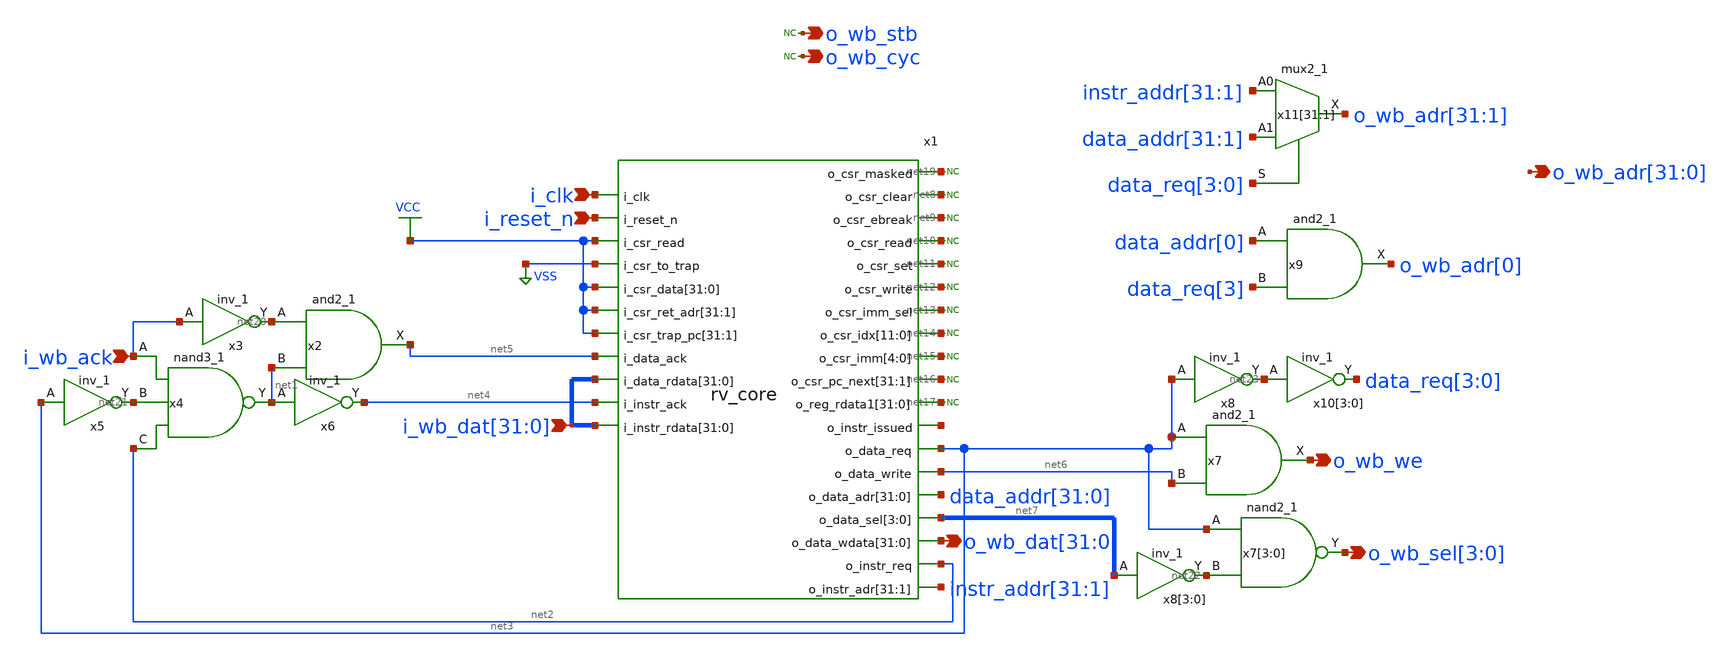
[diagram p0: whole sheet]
** sch_path: blocks/rv_core_wb/rv_core_wb.sch
**.subckt rv_core_wb i_clk i_reset_n i_wb_ack o_wb_we
*+ o_wb_sel[3],o_wb_sel[2],o_wb_sel[1],o_wb_sel[0] o_wb_stb o_wb_cyc
*+ o_wb_adr[31],o_wb_adr[30],o_wb_adr[29],o_wb_adr[28],o_wb_adr[27],o_wb_adr[26],o_wb_adr[25],o_wb_adr[24],o_wb_adr[23],o_wb_adr[22],o_wb_adr[21],o_wb_adr[20],o_wb_adr[19],o_wb_adr[18],o_wb_adr[17],o_wb_adr[16],o_wb_adr[15],o_wb_adr[14],o_wb_adr[13],o_wb_adr[12],o_wb_adr[11],o_wb_adr[10],o_wb_adr[9],o_wb_adr[8],o_wb_adr[7],o_wb_adr[6],o_wb_adr[5],o_wb_adr[4],o_wb_adr[3],o_wb_adr[2],o_wb_adr[1],o_wb_adr[0]
*+ o_wb_dat[31],o_wb_dat[30],o_wb_dat[29],o_wb_dat[28],o_wb_dat[27],o_wb_dat[26],o_wb_dat[25],o_wb_dat[24],o_wb_dat[23],o_wb_dat[22],o_wb_dat[21],o_wb_dat[20],o_wb_dat[19],o_wb_dat[18],o_wb_dat[17],o_wb_dat[16],o_wb_dat[15],o_wb_dat[14],o_wb_dat[13],o_wb_dat[12],o_wb_dat[11],o_wb_dat[10],o_wb_dat[9],o_wb_dat[8],o_wb_dat[7],o_wb_dat[6],o_wb_dat[5],o_wb_dat[4],o_wb_dat[3],o_wb_dat[2],o_wb_dat[1],o_wb_dat[0]
*+ i_wb_dat[31],i_wb_dat[30],i_wb_dat[29],i_wb_dat[28],i_wb_dat[27],i_wb_dat[26],i_wb_dat[25],i_wb_dat[24],i_wb_dat[23],i_wb_dat[22],i_wb_dat[21],i_wb_dat[20],i_wb_dat[19],i_wb_dat[18],i_wb_dat[17],i_wb_dat[16],i_wb_dat[15],i_wb_dat[14],i_wb_dat[13],i_wb_dat[12],i_wb_dat[11],i_wb_dat[10],i_wb_dat[9],i_wb_dat[8],i_wb_dat[7],i_wb_dat[6],i_wb_dat[5],i_wb_dat[4],i_wb_dat[3],i_wb_dat[2],i_wb_dat[1],i_wb_dat[0]
*.ipin i_clk
*.ipin i_reset_n
*.ipin i_wb_ack
*.opin o_wb_we
*.opin o_wb_sel[3],o_wb_sel[2],o_wb_sel[1],o_wb_sel[0]
*.opin o_wb_stb
*.opin o_wb_cyc
*.opin
*+ o_wb_adr[31],o_wb_adr[30],o_wb_adr[29],o_wb_adr[28],o_wb_adr[27],o_wb_adr[26],o_wb_adr[25],o_wb_adr[24],o_wb_adr[23],o_wb_adr[22],o_wb_adr[21],o_wb_adr[20],o_wb_adr[19],o_wb_adr[18],o_wb_adr[17],o_wb_adr[16],o_wb_adr[15],o_wb_adr[14],o_wb_adr[13],o_wb_adr[12],o_wb_adr[11],o_wb_adr[10],o_wb_adr[9],o_wb_adr[8],o_wb_adr[7],o_wb_adr[6],o_wb_adr[5],o_wb_adr[4],o_wb_adr[3],o_wb_adr[2],o_wb_adr[1],o_wb_adr[0]
*.opin
*+ o_wb_dat[31],o_wb_dat[30],o_wb_dat[29],o_wb_dat[28],o_wb_dat[27],o_wb_dat[26],o_wb_dat[25],o_wb_dat[24],o_wb_dat[23],o_wb_dat[22],o_wb_dat[21],o_wb_dat[20],o_wb_dat[19],o_wb_dat[18],o_wb_dat[17],o_wb_dat[16],o_wb_dat[15],o_wb_dat[14],o_wb_dat[13],o_wb_dat[12],o_wb_dat[11],o_wb_dat[10],o_wb_dat[9],o_wb_dat[8],o_wb_dat[7],o_wb_dat[6],o_wb_dat[5],o_wb_dat[4],o_wb_dat[3],o_wb_dat[2],o_wb_dat[1],o_wb_dat[0]
*.ipin
*+ i_wb_dat[31],i_wb_dat[30],i_wb_dat[29],i_wb_dat[28],i_wb_dat[27],i_wb_dat[26],i_wb_dat[25],i_wb_dat[24],i_wb_dat[23],i_wb_dat[22],i_wb_dat[21],i_wb_dat[20],i_wb_dat[19],i_wb_dat[18],i_wb_dat[17],i_wb_dat[16],i_wb_dat[15],i_wb_dat[14],i_wb_dat[13],i_wb_dat[12],i_wb_dat[11],i_wb_dat[10],i_wb_dat[9],i_wb_dat[8],i_wb_dat[7],i_wb_dat[6],i_wb_dat[5],i_wb_dat[4],i_wb_dat[3],i_wb_dat[2],i_wb_dat[1],i_wb_dat[0]
x1 net8 i_clk net9 i_reset_n VCC net10 net11 VSS net12 VCC VCC VCC VCC VCC VCC VCC VCC VCC VCC VCC
+ VCC VCC VCC VCC VCC VCC VCC VCC VCC VCC VCC VCC VCC VCC VCC VCC VCC VCC VCC VCC VCC VCC VCC VCC VCC VCC
+ VCC VCC VCC VCC VCC VCC VCC VCC VCC VCC VCC VCC VCC VCC VCC VCC VCC VCC VCC VCC VCC VCC VCC VCC VCC VCC
+ net13 net14 net14 net14 net14 net14 net14 net14 net14 net14 net14 net14 net14 VCC VCC VCC VCC VCC VCC VCC
+ VCC VCC VCC VCC VCC VCC VCC VCC VCC VCC VCC VCC VCC VCC VCC VCC VCC VCC VCC VCC VCC VCC VCC VCC net15
+ net15 net15 net15 net15 net16 net16 net16 net16 net16 net16 net16 net16 net16 net16 net16 net16 net16
+ net16 net16 net16 net16 net16 net16 net16 net16 net16 net16 net16 net16 net16 net16 net16 net16 net16
+ net16 net17 net17 net17 net17 net17 net17 net17 net17 net17 net17 net17 net17 net17 net17 net17 net17
+ net17 net17 net17 net17 net17 net17 net17 net17 net17 net17 net17 net17 net17 net17 net17 net17 net18
+ net3 net5 net6 i_wb_dat[31] i_wb_dat[30] i_wb_dat[29] i_wb_dat[28] i_wb_dat[27] i_wb_dat[26]
+ i_wb_dat[25] i_wb_dat[24] i_wb_dat[23] i_wb_dat[22] i_wb_dat[21] i_wb_dat[20] i_wb_dat[19] i_wb_dat[18]
+ i_wb_dat[17] i_wb_dat[16] i_wb_dat[15] i_wb_dat[14] i_wb_dat[13] i_wb_dat[12] i_wb_dat[11] i_wb_dat[10]
+ i_wb_dat[9] i_wb_dat[8] i_wb_dat[7] i_wb_dat[6] i_wb_dat[5] i_wb_dat[4] i_wb_dat[3] i_wb_dat[2] i_wb_dat[1]
+ i_wb_dat[0] data_addr[31] data_addr[30] data_addr[29] data_addr[28] data_addr[27] data_addr[26] data_addr[25]
+ data_addr[24] data_addr[23] data_addr[22] data_addr[21] data_addr[20] data_addr[19] data_addr[18] data_addr[17]
+ data_addr[16] data_addr[15] data_addr[14] data_addr[13] data_addr[12] data_addr[11] data_addr[10] data_addr[9]
+ data_addr[8] data_addr[7] data_addr[6] data_addr[5] data_addr[4] data_addr[3] data_addr[2] data_addr[1]
+ data_addr[0] net7[3] net7[2] net7[1] net7[0] o_wb_dat[31] o_wb_dat[30] o_wb_dat[29] o_wb_dat[28] o_wb_dat[27]
+ o_wb_dat[26] o_wb_dat[25] o_wb_dat[24] o_wb_dat[23] o_wb_dat[22] o_wb_dat[21] o_wb_dat[20] o_wb_dat[19]
+ o_wb_dat[18] o_wb_dat[17] o_wb_dat[16] o_wb_dat[15] o_wb_dat[14] o_wb_dat[13] o_wb_dat[12] o_wb_dat[11]
+ o_wb_dat[10] o_wb_dat[9] o_wb_dat[8] o_wb_dat[7] o_wb_dat[6] o_wb_dat[5] o_wb_dat[4] o_wb_dat[3] o_wb_dat[2]
+ o_wb_dat[1] o_wb_dat[0] net2 net4 instr_addr[31] instr_addr[30] instr_addr[29] instr_addr[28] instr_addr[27]
+ instr_addr[26] instr_addr[25] instr_addr[24] instr_addr[23] instr_addr[22] instr_addr[21] instr_addr[20]
+ instr_addr[19] instr_addr[18] instr_addr[17] instr_addr[16] instr_addr[15] instr_addr[14] instr_addr[13]
+ instr_addr[12] instr_addr[11] instr_addr[10] instr_addr[9] instr_addr[8] instr_addr[7] instr_addr[6] instr_addr[5]
+ instr_addr[4] instr_addr[3] instr_addr[2] instr_addr[1] i_wb_dat[31] i_wb_dat[30] i_wb_dat[29] i_wb_dat[28]
+ i_wb_dat[27] i_wb_dat[26] i_wb_dat[25] i_wb_dat[24] i_wb_dat[23] i_wb_dat[22] i_wb_dat[21] i_wb_dat[20]
+ i_wb_dat[19] i_wb_dat[18] i_wb_dat[17] i_wb_dat[16] i_wb_dat[15] i_wb_dat[14] i_wb_dat[13] i_wb_dat[12]
+ i_wb_dat[11] i_wb_dat[10] i_wb_dat[9] i_wb_dat[8] i_wb_dat[7] i_wb_dat[6] i_wb_dat[5] i_wb_dat[4] i_wb_dat[3]
+ i_wb_dat[2] i_wb_dat[1] i_wb_dat[0] net19 rv_core
x2 net20 net1 VSS VSS VCC VCC net5 sky130_fd_sc_hs__and2_1
x3 i_wb_ack VSS VSS VCC VCC net20 sky130_fd_sc_hs__inv_1
x4 i_wb_ack net21 net2 VSS VSS VCC VCC net1 sky130_fd_sc_hs__nand3_1
x5 net3 VSS VSS VCC VCC net21 sky130_fd_sc_hs__inv_1
x6 net1 VSS VSS VCC VCC net4 sky130_fd_sc_hs__inv_1
* noconn #net8
* noconn #net9
* noconn #net10
* noconn #net11
* noconn #net12
* noconn #net13
* noconn #net14
* noconn #net15
* noconn #net16
* noconn #net17
x7 net3 net6 VSS VSS VCC VCC o_wb_we sky130_fd_sc_hs__and2_1
x8[3] net7[3] VSS VSS VCC VCC net22[3] sky130_fd_sc_hs__inv_1
x8[2] net7[2] VSS VSS VCC VCC net22[2] sky130_fd_sc_hs__inv_1
x8[1] net7[1] VSS VSS VCC VCC net22[1] sky130_fd_sc_hs__inv_1
x8[0] net7[0] VSS VSS VCC VCC net22[0] sky130_fd_sc_hs__inv_1
x7[3] net3 net22[3] VSS VSS VCC VCC o_wb_sel[3] sky130_fd_sc_hs__nand2_1
x7[2] net3 net22[2] VSS VSS VCC VCC o_wb_sel[2] sky130_fd_sc_hs__nand2_1
x7[1] net3 net22[1] VSS VSS VCC VCC o_wb_sel[1] sky130_fd_sc_hs__nand2_1
x7[0] net3 net22[0] VSS VSS VCC VCC o_wb_sel[0] sky130_fd_sc_hs__nand2_1
x8 net3 VSS VSS VCC VCC net23 sky130_fd_sc_hs__inv_1
x10[3] net23 VSS VSS VCC VCC data_req[3] sky130_fd_sc_hs__inv_1
x10[2] net23 VSS VSS VCC VCC data_req[2] sky130_fd_sc_hs__inv_1
x10[1] net23 VSS VSS VCC VCC data_req[1] sky130_fd_sc_hs__inv_1
x10[0] net23 VSS VSS VCC VCC data_req[0] sky130_fd_sc_hs__inv_1
x9 data_addr[0] data_req[3] VSS VSS VCC VCC o_wb_adr[0] sky130_fd_sc_hs__and2_1
x11[31] instr_addr[31] data_addr[31] data_req[3] VSS VSS VCC VCC o_wb_adr[31]
+ sky130_fd_sc_hs__mux2_1
x11[30] instr_addr[30] data_addr[30] data_req[2] VSS VSS VCC VCC o_wb_adr[30]
+ sky130_fd_sc_hs__mux2_1
x11[29] instr_addr[29] data_addr[29] data_req[1] VSS VSS VCC VCC o_wb_adr[29]
+ sky130_fd_sc_hs__mux2_1
x11[28] instr_addr[28] data_addr[28] data_req[0] VSS VSS VCC VCC o_wb_adr[28]
+ sky130_fd_sc_hs__mux2_1
x11[27] instr_addr[27] data_addr[27] data_req[3] VSS VSS VCC VCC o_wb_adr[27]
+ sky130_fd_sc_hs__mux2_1
x11[26] instr_addr[26] data_addr[26] data_req[2] VSS VSS VCC VCC o_wb_adr[26]
+ sky130_fd_sc_hs__mux2_1
x11[25] instr_addr[25] data_addr[25] data_req[1] VSS VSS VCC VCC o_wb_adr[25]
+ sky130_fd_sc_hs__mux2_1
x11[24] instr_addr[24] data_addr[24] data_req[0] VSS VSS VCC VCC o_wb_adr[24]
+ sky130_fd_sc_hs__mux2_1
x11[23] instr_addr[23] data_addr[23] data_req[3] VSS VSS VCC VCC o_wb_adr[23]
+ sky130_fd_sc_hs__mux2_1
x11[22] instr_addr[22] data_addr[22] data_req[2] VSS VSS VCC VCC o_wb_adr[22]
+ sky130_fd_sc_hs__mux2_1
x11[21] instr_addr[21] data_addr[21] data_req[1] VSS VSS VCC VCC o_wb_adr[21]
+ sky130_fd_sc_hs__mux2_1
x11[20] instr_addr[20] data_addr[20] data_req[0] VSS VSS VCC VCC o_wb_adr[20]
+ sky130_fd_sc_hs__mux2_1
x11[19] instr_addr[19] data_addr[19] data_req[3] VSS VSS VCC VCC o_wb_adr[19]
+ sky130_fd_sc_hs__mux2_1
x11[18] instr_addr[18] data_addr[18] data_req[2] VSS VSS VCC VCC o_wb_adr[18]
+ sky130_fd_sc_hs__mux2_1
x11[17] instr_addr[17] data_addr[17] data_req[1] VSS VSS VCC VCC o_wb_adr[17]
+ sky130_fd_sc_hs__mux2_1
x11[16] instr_addr[16] data_addr[16] data_req[0] VSS VSS VCC VCC o_wb_adr[16]
+ sky130_fd_sc_hs__mux2_1
x11[15] instr_addr[15] data_addr[15] data_req[3] VSS VSS VCC VCC o_wb_adr[15]
+ sky130_fd_sc_hs__mux2_1
x11[14] instr_addr[14] data_addr[14] data_req[2] VSS VSS VCC VCC o_wb_adr[14]
+ sky130_fd_sc_hs__mux2_1
x11[13] instr_addr[13] data_addr[13] data_req[1] VSS VSS VCC VCC o_wb_adr[13]
+ sky130_fd_sc_hs__mux2_1
x11[12] instr_addr[12] data_addr[12] data_req[0] VSS VSS VCC VCC o_wb_adr[12]
+ sky130_fd_sc_hs__mux2_1
x11[11] instr_addr[11] data_addr[11] data_req[3] VSS VSS VCC VCC o_wb_adr[11]
+ sky130_fd_sc_hs__mux2_1
x11[10] instr_addr[10] data_addr[10] data_req[2] VSS VSS VCC VCC o_wb_adr[10]
+ sky130_fd_sc_hs__mux2_1
x11[9] instr_addr[9] data_addr[9] data_req[1] VSS VSS VCC VCC o_wb_adr[9] sky130_fd_sc_hs__mux2_1
x11[8] instr_addr[8] data_addr[8] data_req[0] VSS VSS VCC VCC o_wb_adr[8] sky130_fd_sc_hs__mux2_1
x11[7] instr_addr[7] data_addr[7] data_req[3] VSS VSS VCC VCC o_wb_adr[7] sky130_fd_sc_hs__mux2_1
x11[6] instr_addr[6] data_addr[6] data_req[2] VSS VSS VCC VCC o_wb_adr[6] sky130_fd_sc_hs__mux2_1
x11[5] instr_addr[5] data_addr[5] data_req[1] VSS VSS VCC VCC o_wb_adr[5] sky130_fd_sc_hs__mux2_1
x11[4] instr_addr[4] data_addr[4] data_req[0] VSS VSS VCC VCC o_wb_adr[4] sky130_fd_sc_hs__mux2_1
x11[3] instr_addr[3] data_addr[3] data_req[3] VSS VSS VCC VCC o_wb_adr[3] sky130_fd_sc_hs__mux2_1
x11[2] instr_addr[2] data_addr[2] data_req[2] VSS VSS VCC VCC o_wb_adr[2] sky130_fd_sc_hs__mux2_1
x11[1] instr_addr[1] data_addr[1] data_req[1] VSS VSS VCC VCC o_wb_adr[1] sky130_fd_sc_hs__mux2_1
* noconn o_wb_cyc
* noconn o_wb_stb
* noconn #net19
**.ends
.GLOBAL VCC
.GLOBAL VSS
.end
